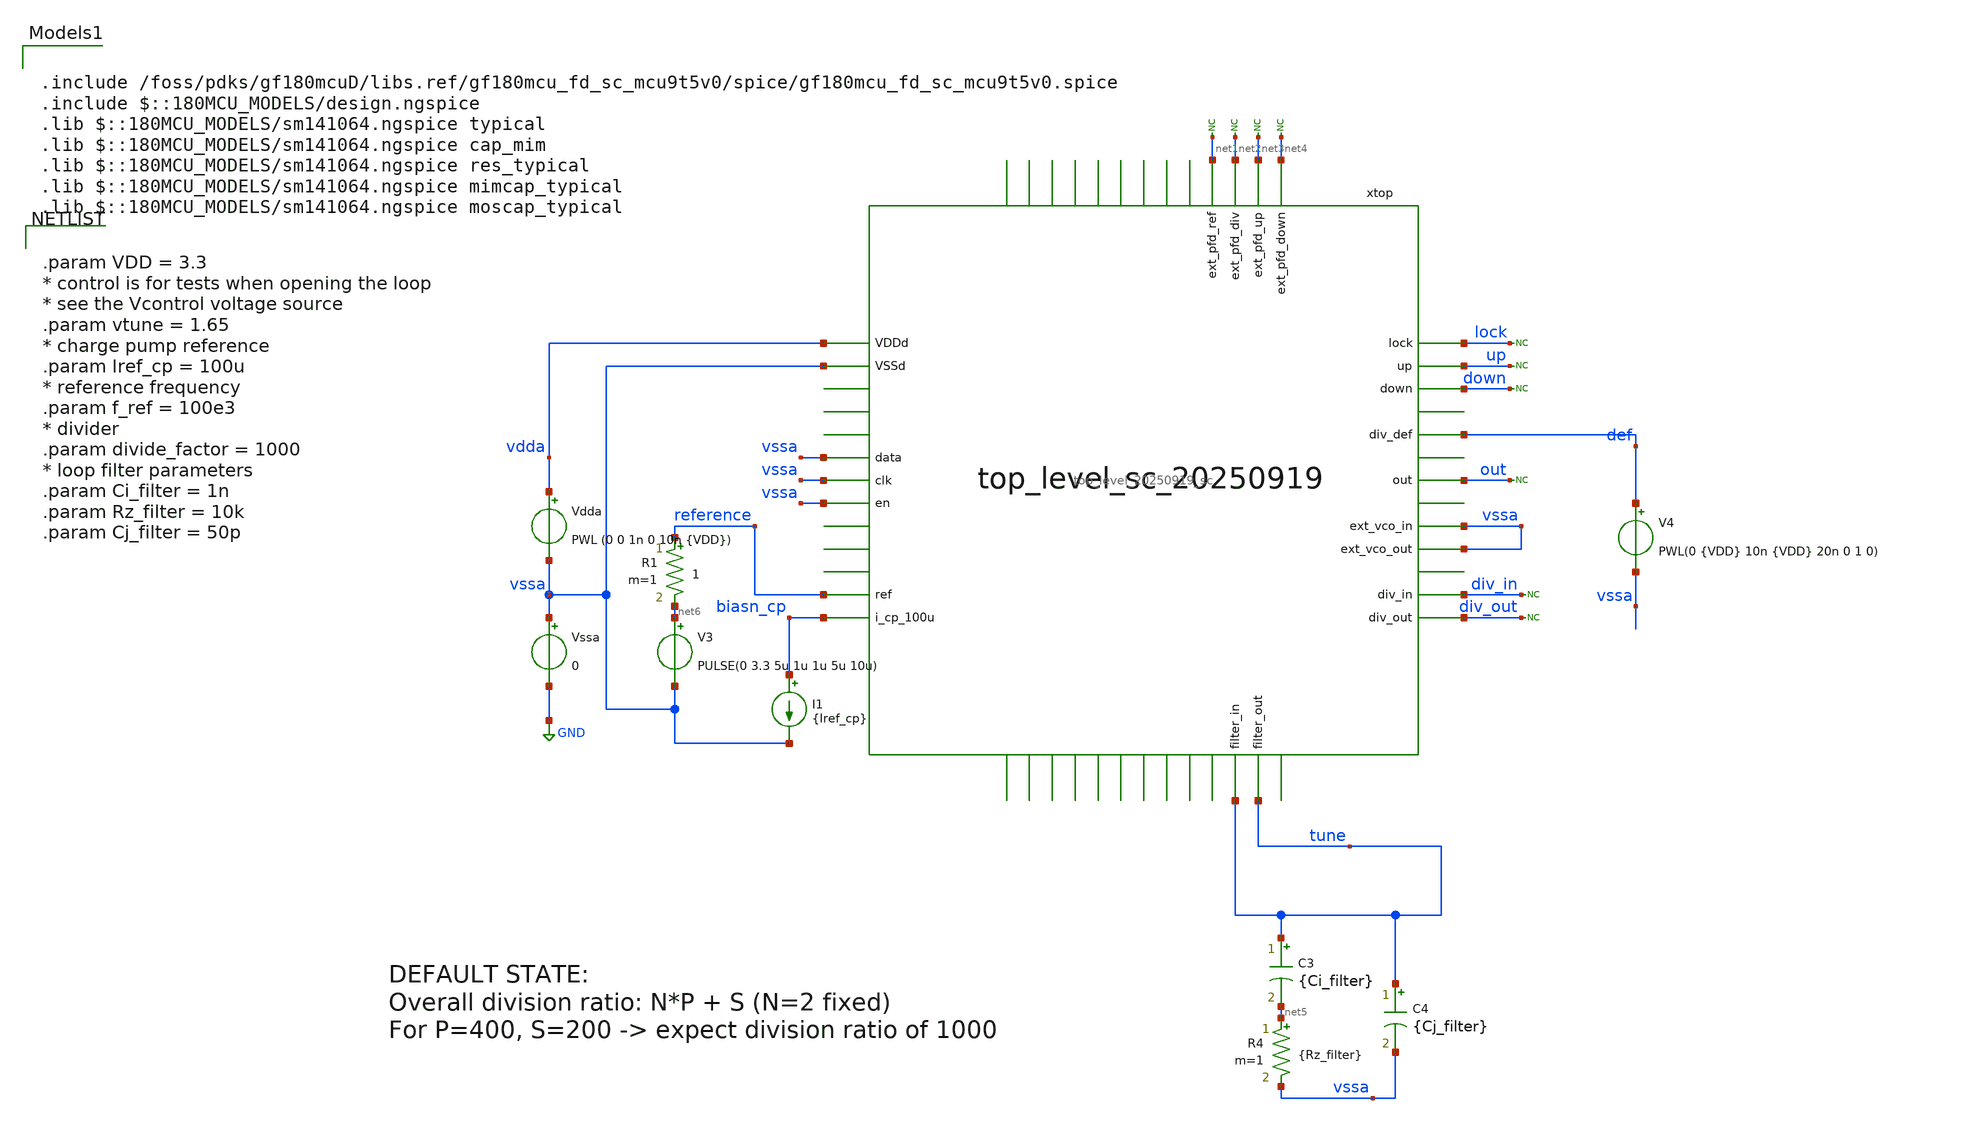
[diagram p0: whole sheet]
** sch_path: designs/libs/tb_top_level/tb_top_level_20250919_sc.sch
**.subckt tb_top_level_20250919_sc
Vssa vssa GND 0
Vdda vdda vssa PWL (0 0 1n 0 10n {VDD})
V4 def vssa PWL(0 {VDD} 10n {VDD} 20n 0 1 0)
* noconn #net1
* noconn #net2
* noconn #net3
* noconn #net4
* noconn div_in
* noconn div_out
* noconn down
* noconn up
* noconn lock
C3 tune net5 {Ci_filter} m=1
R4 net5 vssa {Rz_filter} m=1
C4 tune vssa {Cj_filter} m=1
* noconn out
V3 net6 vssa PULSE(0 3.3 5u 1u 1u 5u 10u)
R1 reference net6 1 m=1
I1 biasn_cp vssa {Iref_cp}
xtop vdda vssa vssa vssa vssa reference biasn_cp net1 net2 net3 net4 lock up down tune vssa div_in
+ div_out out tune vssa def top_level_20250919_sc
**** begin user architecture code


.param VDD = 3.3
* control is for tests when opening the loop
* see the Vcontrol voltage source
.param vtune = 1.65
* charge pump reference
.param Iref_cp = 100u
* reference frequency
.param f_ref = 100e3
* divider
.param divide_factor = 1000
* loop filter parameters
.param Ci_filter = 1n
.param Rz_filter = 10k
.param Cj_filter = 50p



.include /foss/pdks/gf180mcuD/libs.ref/gf180mcu_fd_sc_mcu9t5v0/spice/gf180mcu_fd_sc_mcu9t5v0.spice
.include $::180MCU_MODELS/design.ngspice
.lib $::180MCU_MODELS/sm141064.ngspice typical
.lib $::180MCU_MODELS/sm141064.ngspice cap_mim
.lib $::180MCU_MODELS/sm141064.ngspice res_typical
.lib $::180MCU_MODELS/sm141064.ngspice mimcap_typical
.lib $::180MCU_MODELS/sm141064.ngspice moscap_typical



.save v(tune) v(out) v(reference) v(up) v(down) v(xtop.xtop_nosc.int_div_out) v(xtop.xtop_nosc.int_div_in) v(xtop.xtop_nosc.dff_pfd_ref) v(xtop.xtop_nosc.dff_pfd_up) v(xtop.xtop_nosc.up_pre) v(xtop.xtop_nosc.up_post) v(xtop.xtop_nosc.down_pre) v(xtop.xtop_nosc.down_post) v(lock)
.save v(xtop.xtop_nosc.xpfd.x1.rst) v(xtop.xtop_nosc.xpfd.x1.net2) v(xtop.xtop_nosc.xpfd.x1.net3) v(xtop.xtop_nosc.xpfd.x1.net4) v(xtop.xtop_nosc.xpfd.x1.net6)
.save v(xtop.xtop_nosc.xpfd.x1.net5) v(xtop.xtop_nosc.xpfd.x1.Qb) v(xtop.xtop_nosc.xpfd.x1.clka) v(xtop.xtop_nosc.xpfd.x1.clkb)

.control
set filetype=raw
tran 1n 200u
write tb_top_level_20250912_sc.raw
.endc


**** end user architecture code
**.ends
.GLOBAL GND
.end
